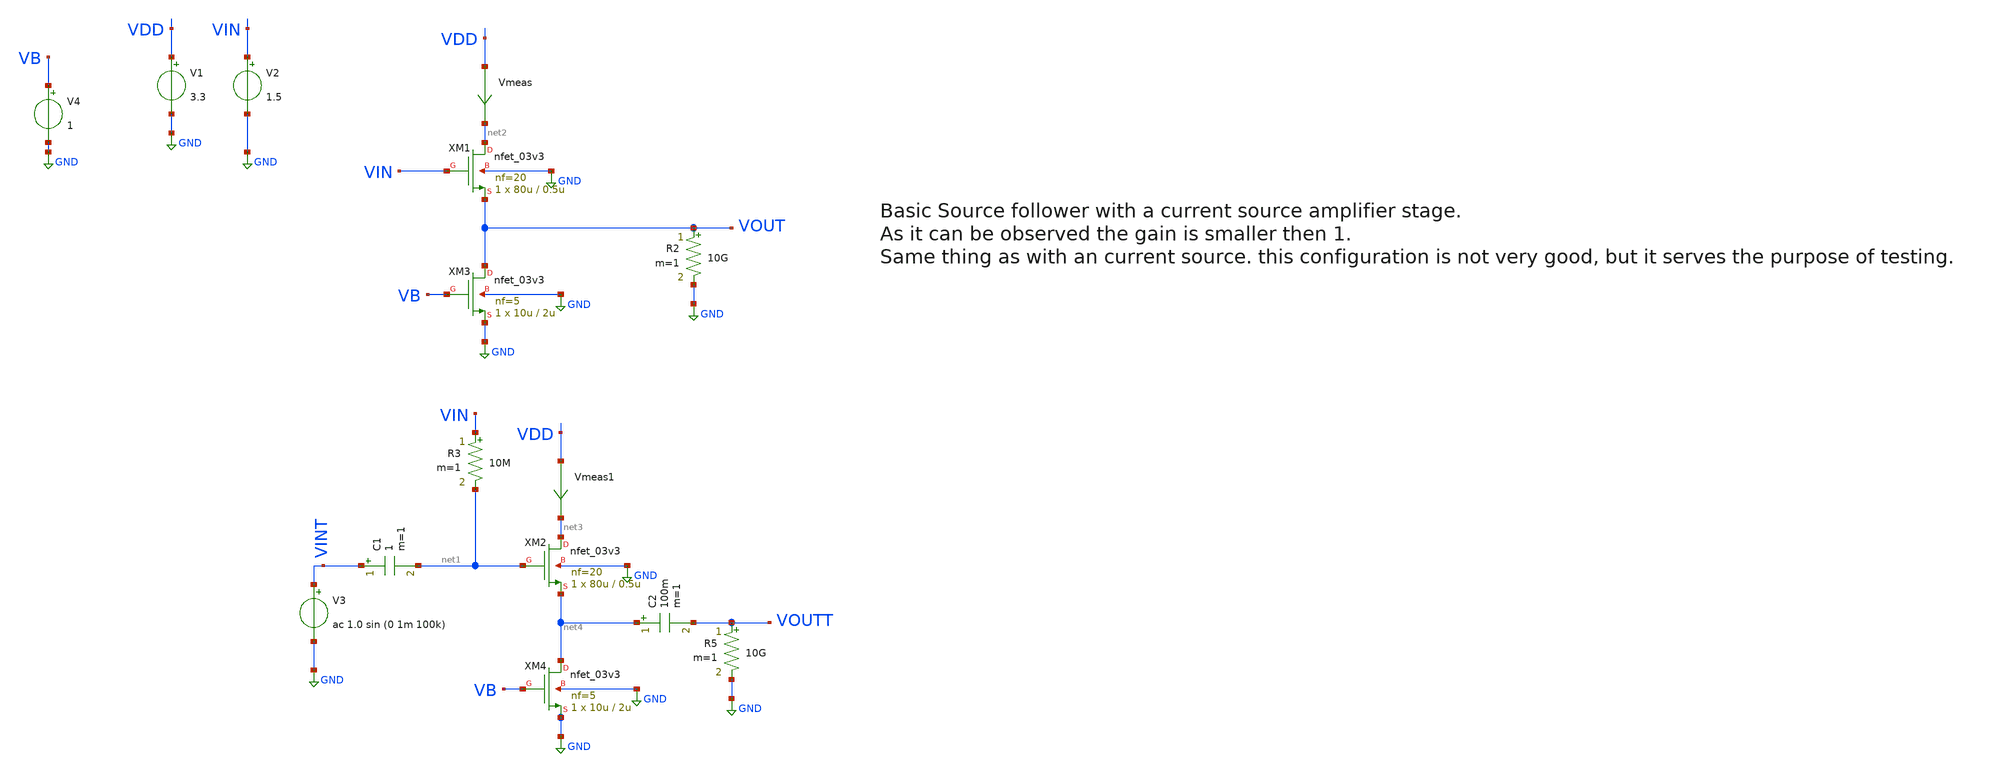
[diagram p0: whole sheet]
** sch_path: basic_circuits/source_follower_current_source.sch
**.subckt source_follower_current_source
XM1 net2 VIN VOUT GND nfet_03v3 L=0.5u W=80u nf=20 ad='int((nf+1)/2) * W/nf * 0.18u' as='int((nf+2)/2) * W/nf * 0.18u'
+ pd='2*int((nf+1)/2) * (W/nf + 0.18u)' ps='2*int((nf+2)/2) * (W/nf + 0.18u)' nrd='0.18u / W' nrs='0.18u / W'
+ sa=0 sb=0 sd=0 m=1
Vmeas VDD net2 0
.save i(vmeas)
V1 VDD GND 3.3
V2 VIN GND 1.5
V3 VINT GND ac 1.0 sin (0 1m 100k)
R2 VOUT GND 10G m=1
C1 VINT net1 1 m=1
R3 VIN net1 10M m=1
C2 net4 VOUTT 100m m=1
R5 VOUTT GND 10G m=1
XM2 net3 net1 net4 GND nfet_03v3 L=0.5u W=80u nf=20 ad='int((nf+1)/2) * W/nf * 0.18u' as='int((nf+2)/2) * W/nf * 0.18u'
+ pd='2*int((nf+1)/2) * (W/nf + 0.18u)' ps='2*int((nf+2)/2) * (W/nf + 0.18u)' nrd='0.18u / W' nrs='0.18u / W'
+ sa=0 sb=0 sd=0 m=1
Vmeas1 VDD net3 0
.save i(vmeas1)
XM3 VOUT VB GND GND nfet_03v3 L=2u W=10u nf=5 ad='int((nf+1)/2) * W/nf * 0.18u' as='int((nf+2)/2) * W/nf * 0.18u'
+ pd='2*int((nf+1)/2) * (W/nf + 0.18u)' ps='2*int((nf+2)/2) * (W/nf + 0.18u)' nrd='0.18u / W' nrs='0.18u / W'
+ sa=0 sb=0 sd=0 m=1
V4 VB GND 1
XM4 net4 VB GND GND nfet_03v3 L=2u W=10u nf=5 ad='int((nf+1)/2) * W/nf * 0.18u' as='int((nf+2)/2) * W/nf * 0.18u'
+ pd='2*int((nf+1)/2) * (W/nf + 0.18u)' ps='2*int((nf+2)/2) * (W/nf + 0.18u)' nrd='0.18u / W' nrs='0.18u / W'
+ sa=0 sb=0 sd=0 m=1
**** begin user architecture code

**************************************************************
**************************************************************
**************************************************************
**************************************************************
**************************************************************
*LIBs*********************************************************
**************************************************************
**************************************************************
**************************************************************
**************************************************************
**************************************************************
.include $::180MCU_MODELS/design.ngspice
*.lib $::180MCU_MODELS/sm141064.ngspice statistical *use statistical if you want global and parameter mismatch
*.lib $::180MCU_MODELS/sm141064.ngspice res_statistical
.lib $::180MCU_MODELS/sm141064.ngspice typical
.lib $::180MCU_MODELS/sm141064.ngspice res_typical
.lib $::180MCU_MODELS/sm141064.ngspice moscap_typical
.lib $::180MCU_MODELS/sm141064.ngspice bjt_typical
.lib $::180MCU_MODELS/sm141064.ngspice diode_typical
.lib $::180MCU_MODELS/sm141064.ngspice mimcap_typical
**************************************************************
**************************************************************
**************************************************************
**************************************************************
**************************************************************
*Corners/montecarlo options***********************************
**************************************************************
**************************************************************
**************************************************************
**************************************************************
**************************************************************
.TEMP 27
.param   sw_stat_global = 1   sw_stat_mism = 1  mc_skew = 3  res_mc_skew = 3  cap_mc_skew = 3
+  fnoicor = 1
**************************************************************
**************************************************************
**************************************************************
**************************************************************
*SIMULATION and Plots*****************************************
**************************************************************
**************************************************************
**************************************************************
**************************************************************
.control
save all
dc V2 0 3.3 0.01
*dc simulation
plot v(VOUT) v(VIN) deriv(v(VOUT))
*ploting VIN VOUT and the voltage gain
plot i(Vmeas)
*ploting the current for curiosity
tran 1ns 20u
*transient simulation
plot (v(VINT)) (v(VOUTT))
*simple plot to exemplify the gain
fft v(VOUTT) v(VINT)
*fast fourier transfor
plot mag(v(VOUTT)) mag(v(VINT))
* analyse the frequency spectrum of the transient waves, to detect distortion
ac dec 20 1 50G
*simple ac simulation
plot v(VOUTT)
*gain in function of the input frequency
.endc

**** end user architecture code
**.ends
.GLOBAL GND
.end
